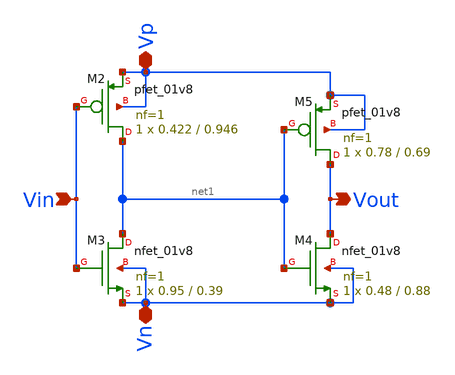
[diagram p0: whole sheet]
** sch_path: xschem/Vth_sch/Symbol/th01.sch
**.subckt th01 Vin Vout Vp Vn
*.ipin Vin
*.opin Vout
*.iopin Vp
*.iopin Vn
XM5 Vout net1 Vp Vp sky130_fd_pr__pfet_01v8 L=0.69 W=0.78 nf=1 ad='int((nf+1)/2) * W/nf * 0.29' as='int((nf+2)/2) * W/nf * 0.29'
+ pd='2*int((nf+1)/2) * (W/nf + 0.29)' ps='2*int((nf+2)/2) * (W/nf + 0.29)' nrd='0.29 / W' nrs='0.29 / W'
+ sa=0 sb=0 sd=0 mult=1 m=1
XM4 Vout net1 Vn Vn sky130_fd_pr__nfet_01v8 L=0.88 W=0.48 nf=1 ad='int((nf+1)/2) * W/nf * 0.29' as='int((nf+2)/2) * W/nf * 0.29'
+ pd='2*int((nf+1)/2) * (W/nf + 0.29)' ps='2*int((nf+2)/2) * (W/nf + 0.29)' nrd='0.29 / W' nrs='0.29 / W'
+ sa=0 sb=0 sd=0 mult=1 m=1
XM2 net1 Vin Vp Vp sky130_fd_pr__pfet_01v8 L=0.946 W=0.422 nf=1 ad='int((nf+1)/2) * W/nf * 0.29' as='int((nf+2)/2) * W/nf * 0.29'
+ pd='2*int((nf+1)/2) * (W/nf + 0.29)' ps='2*int((nf+2)/2) * (W/nf + 0.29)' nrd='0.29 / W' nrs='0.29 / W'
+ sa=0 sb=0 sd=0 mult=1 m=1
XM3 net1 Vin Vn Vn sky130_fd_pr__nfet_01v8 L=0.39 W=0.95 nf=1 ad='int((nf+1)/2) * W/nf * 0.29' as='int((nf+2)/2) * W/nf * 0.29'
+ pd='2*int((nf+1)/2) * (W/nf + 0.29)' ps='2*int((nf+2)/2) * (W/nf + 0.29)' nrd='0.29 / W' nrs='0.29 / W'
+ sa=0 sb=0 sd=0 mult=1 m=1
**.ends
.end
